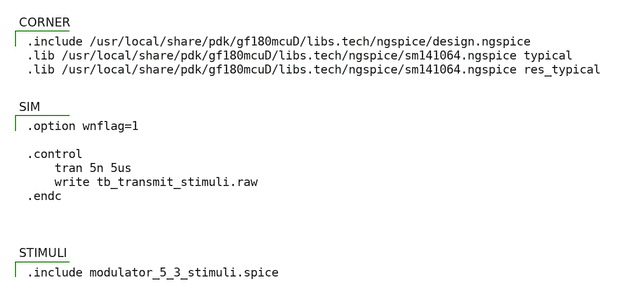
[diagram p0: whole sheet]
** sch_path: xschem/tb_transmit_stimulus_only.sch
**.subckt tb_transmit_stimulus_only
**** begin user architecture code

.include /usr/local/share/pdk/gf180mcuD/libs.tech/ngspice/design.ngspice
.lib /usr/local/share/pdk/gf180mcuD/libs.tech/ngspice/sm141064.ngspice typical
.lib /usr/local/share/pdk/gf180mcuD/libs.tech/ngspice/sm141064.ngspice res_typical


.include modulator_5_3_stimuli.spice


.option wnflag=1

.control
    tran 5n 5us
    write tb_transmit_stimuli.raw
.endc


**** end user architecture code
**.ends
.end
